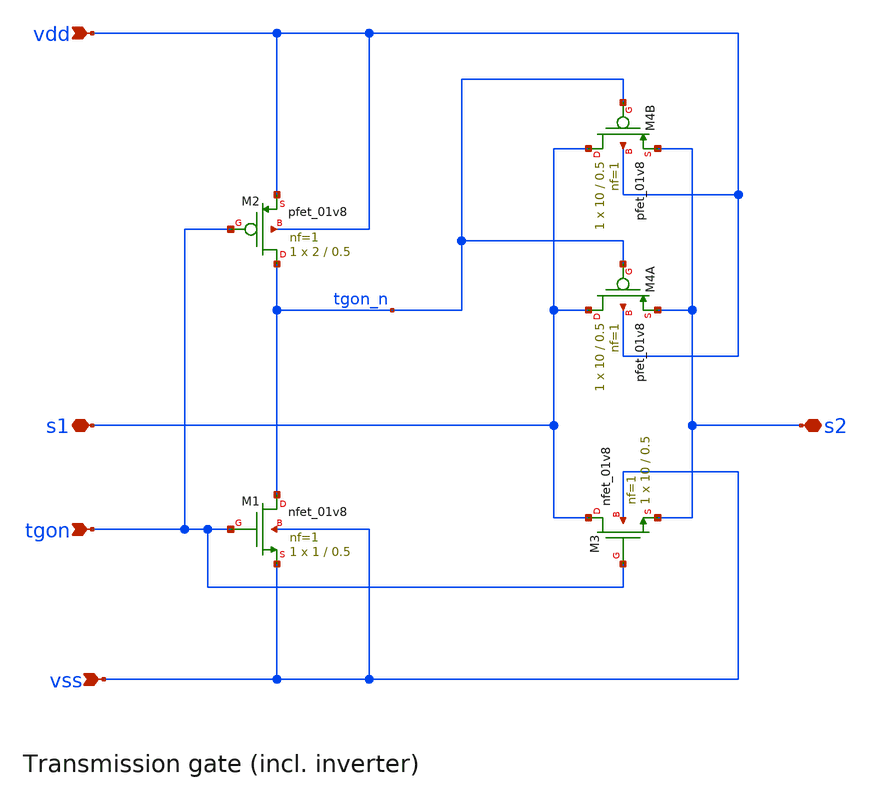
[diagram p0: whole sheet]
** sch_path: xschem/tg.sch
**.subckt tg vdd vss tgon s2 s1
*.ipin vdd
*.ipin vss
*.ipin tgon
*.iopin s2
*.iopin s1
XM3 s1 tgon s2 vss sky130_fd_pr__nfet_01v8 L=0.5 W=10 nf=1 ad='int((nf+1)/2) * W/nf * 0.29' as='int((nf+2)/2) * W/nf * 0.29'
+ pd='2*int((nf+1)/2) * (W/nf + 0.29)' ps='2*int((nf+2)/2) * (W/nf + 0.29)' nrd='0.29 / W' nrs='0.29 / W'
+ sa=0 sb=0 sd=0 mult=1 m=1
XM4A s1 tgon_n s2 vdd sky130_fd_pr__pfet_01v8 L=0.5 W=10 nf=1 ad='int((nf+1)/2) * W/nf * 0.29' as='int((nf+2)/2) * W/nf * 0.29'
+ pd='2*int((nf+1)/2) * (W/nf + 0.29)' ps='2*int((nf+2)/2) * (W/nf + 0.29)' nrd='0.29 / W' nrs='0.29 / W'
+ sa=0 sb=0 sd=0 mult=1 m=1
XM4B s1 tgon_n s2 vdd sky130_fd_pr__pfet_01v8 L=0.5 W=10 nf=1 ad='int((nf+1)/2) * W/nf * 0.29' as='int((nf+2)/2) * W/nf * 0.29'
+ pd='2*int((nf+1)/2) * (W/nf + 0.29)' ps='2*int((nf+2)/2) * (W/nf + 0.29)' nrd='0.29 / W' nrs='0.29 / W'
+ sa=0 sb=0 sd=0 mult=1 m=1
XM1 tgon_n tgon vss vss sky130_fd_pr__nfet_01v8 L=0.5 W=1 nf=1 ad='int((nf+1)/2) * W/nf * 0.29' as='int((nf+2)/2) * W/nf * 0.29'
+ pd='2*int((nf+1)/2) * (W/nf + 0.29)' ps='2*int((nf+2)/2) * (W/nf + 0.29)' nrd='0.29 / W' nrs='0.29 / W'
+ sa=0 sb=0 sd=0 mult=1 m=1
XM2 tgon_n tgon vdd vdd sky130_fd_pr__pfet_01v8 L=0.5 W=2 nf=1 ad='int((nf+1)/2) * W/nf * 0.29' as='int((nf+2)/2) * W/nf * 0.29'
+ pd='2*int((nf+1)/2) * (W/nf + 0.29)' ps='2*int((nf+2)/2) * (W/nf + 0.29)' nrd='0.29 / W' nrs='0.29 / W'
+ sa=0 sb=0 sd=0 mult=1 m=1
**.ends
.end
